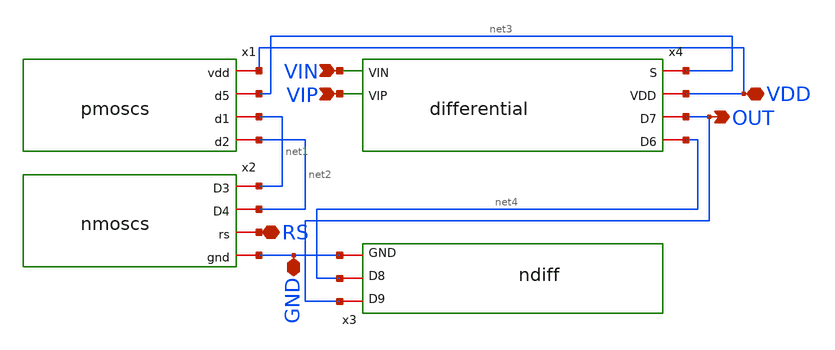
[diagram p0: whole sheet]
** sch_path: opamp1/mag/opamp1.sch
**.subckt opamp1 VIN VIP VDD GND RS OUT
*.ipin VIN
*.ipin VIP
*.iopin VDD
*.iopin GND
*.iopin RS
*.opin OUT
x1 VDD net3 net1 net2 pmoscs
x2 net1 net2 RS GND nmoscs
x3 OUT net4 GND ndiff
x4 net3 VIN VDD VIP OUT net4 differential
**.ends
.end
